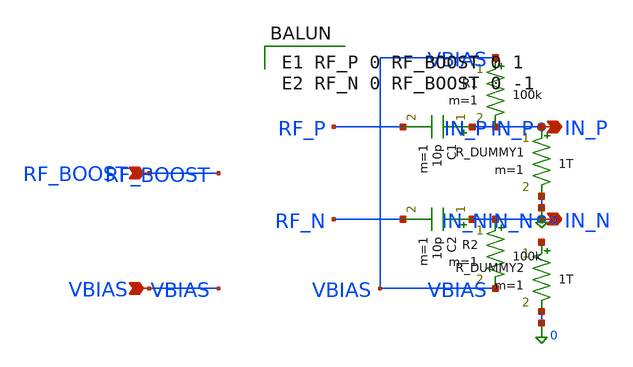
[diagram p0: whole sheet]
** sch_path: modules/PandaChip/designs/iris-harvester/exp/splitter.sch
**.subckt splitter RF_BOOST VBIAS IN_P IN_N
*.ipin RF_BOOST
*.ipin VBIAS
*.opin IN_P
*.opin IN_N
R_DUMMY1 IN_P 0 1T m=1
R_DUMMY2 net1 0 1T m=1
C1 IN_P RF_P 10p m=1
C2 IN_N RF_N 10p m=1
R1 VBIAS IN_P 100k m=1
R2 IN_N VBIAS 100k m=1
**** begin user architecture code

E1 RF_P 0 RF_BOOST 0 1
E2 RF_N 0 RF_BOOST 0 -1

**** end user architecture code
**.ends
.end
